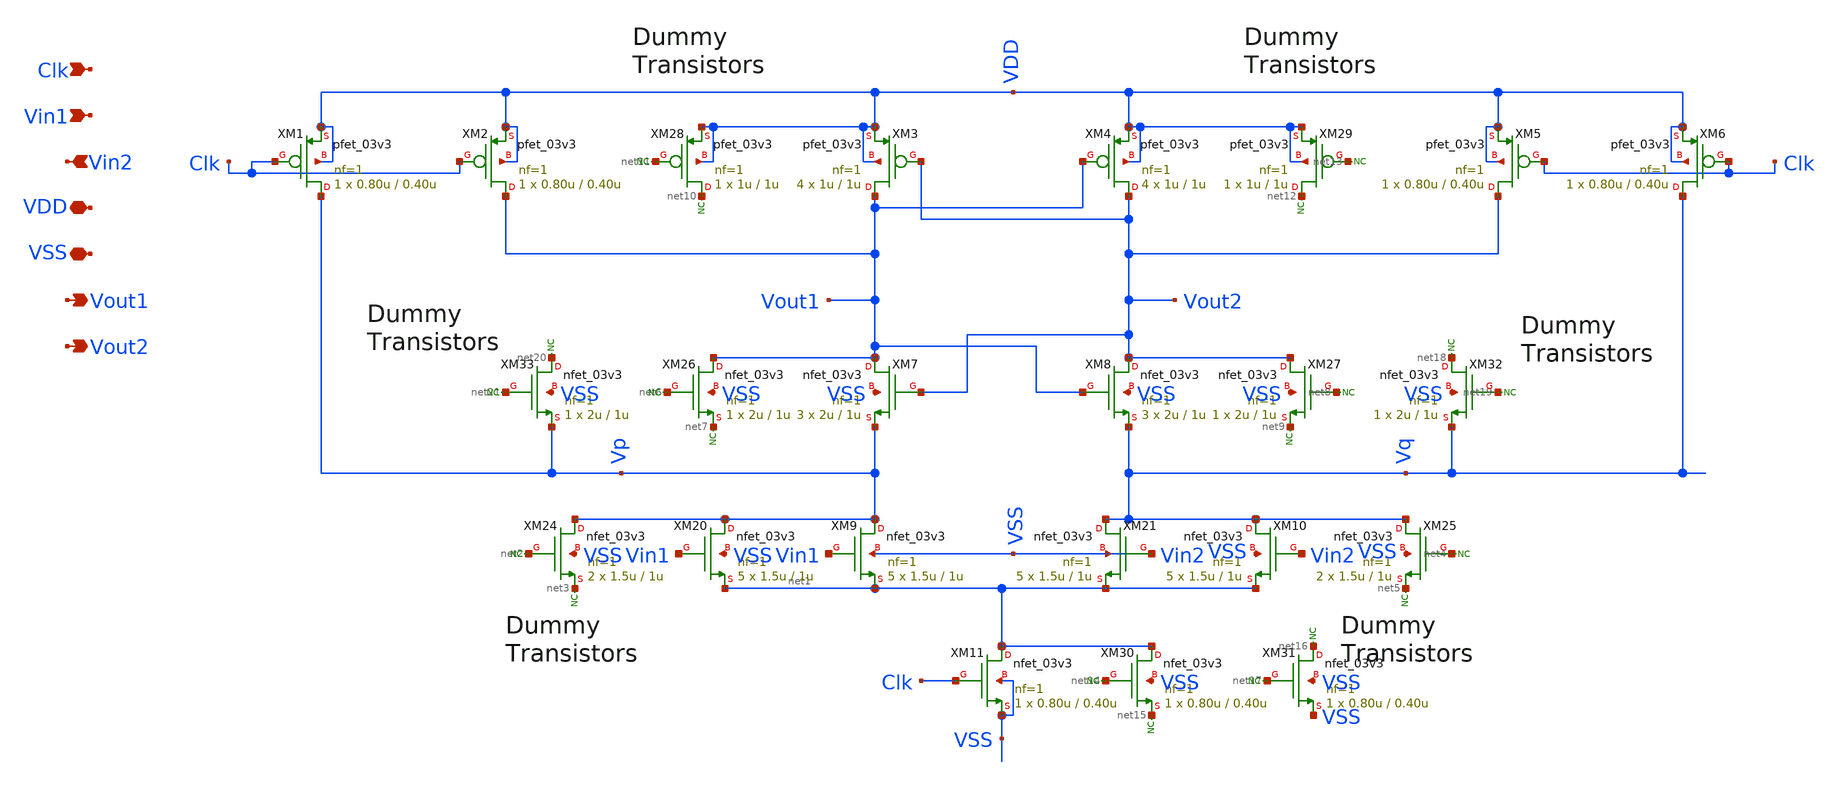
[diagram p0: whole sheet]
** sch_path: designs/FinalBlocksLayout/no_offsetLatch/no_offsetLatch.sch
**.subckt no_offsetLatch Clk Vin1 Vin2 VDD VSS Vout1 Vout2
*.ipin Clk
*.ipin Vin1
*.ipin Vin2
*.iopin VDD
*.iopin VSS
*.opin Vout1
*.opin Vout2
XM1 Vp Clk VDD VDD pfet_03v3 L=0.40u W=0.80u nf=1 ad='int((nf+1)/2) * W/nf * 0.18u' as='int((nf+2)/2) * W/nf * 0.18u'
+ pd='2*int((nf+1)/2) * (W/nf + 0.18u)' ps='2*int((nf+2)/2) * (W/nf + 0.18u)' nrd='0.18u / W' nrs='0.18u / W'
+ sa=0 sb=0 sd=0 m=1
XM2 Vout1 Clk VDD VDD pfet_03v3 L=0.40u W=0.80u nf=1 ad='int((nf+1)/2) * W/nf * 0.18u' as='int((nf+2)/2) * W/nf * 0.18u'
+ pd='2*int((nf+1)/2) * (W/nf + 0.18u)' ps='2*int((nf+2)/2) * (W/nf + 0.18u)' nrd='0.18u / W' nrs='0.18u / W'
+ sa=0 sb=0 sd=0 m=1
XM3 Vout1 Vout2 VDD VDD pfet_03v3 L=1u W=1u nf=1 ad='int((nf+1)/2) * W/nf * 0.18u' as='int((nf+2)/2) * W/nf * 0.18u'
+ pd='2*int((nf+1)/2) * (W/nf + 0.18u)' ps='2*int((nf+2)/2) * (W/nf + 0.18u)' nrd='0.18u / W' nrs='0.18u / W'
+ sa=0 sb=0 sd=0 m=4
XM4 Vout2 Vout1 VDD VDD pfet_03v3 L=1u W=1u nf=1 ad='int((nf+1)/2) * W/nf * 0.18u' as='int((nf+2)/2) * W/nf * 0.18u'
+ pd='2*int((nf+1)/2) * (W/nf + 0.18u)' ps='2*int((nf+2)/2) * (W/nf + 0.18u)' nrd='0.18u / W' nrs='0.18u / W'
+ sa=0 sb=0 sd=0 m=4
XM5 Vout2 Clk VDD VDD pfet_03v3 L=0.40u W=0.80u nf=1 ad='int((nf+1)/2) * W/nf * 0.18u' as='int((nf+2)/2) * W/nf * 0.18u'
+ pd='2*int((nf+1)/2) * (W/nf + 0.18u)' ps='2*int((nf+2)/2) * (W/nf + 0.18u)' nrd='0.18u / W' nrs='0.18u / W'
+ sa=0 sb=0 sd=0 m=1
XM6 Vq Clk VDD VDD pfet_03v3 L=0.40u W=0.80u nf=1 ad='int((nf+1)/2) * W/nf * 0.18u' as='int((nf+2)/2) * W/nf * 0.18u'
+ pd='2*int((nf+1)/2) * (W/nf + 0.18u)' ps='2*int((nf+2)/2) * (W/nf + 0.18u)' nrd='0.18u / W' nrs='0.18u / W'
+ sa=0 sb=0 sd=0 m=1
XM7 Vout1 Vout2 Vp VSS nfet_03v3 L=1u W=2u nf=1 ad='int((nf+1)/2) * W/nf * 0.18u' as='int((nf+2)/2) * W/nf * 0.18u'
+ pd='2*int((nf+1)/2) * (W/nf + 0.18u)' ps='2*int((nf+2)/2) * (W/nf + 0.18u)' nrd='0.18u / W' nrs='0.18u / W'
+ sa=0 sb=0 sd=0 m=3
XM8 Vout2 Vout1 Vq VSS nfet_03v3 L=1u W=2u nf=1 ad='int((nf+1)/2) * W/nf * 0.18u' as='int((nf+2)/2) * W/nf * 0.18u'
+ pd='2*int((nf+1)/2) * (W/nf + 0.18u)' ps='2*int((nf+2)/2) * (W/nf + 0.18u)' nrd='0.18u / W' nrs='0.18u / W'
+ sa=0 sb=0 sd=0 m=3
XM9 Vp Vin1 net1 VSS nfet_03v3 L=1u W=1.5u nf=1 ad='int((nf+1)/2) * W/nf * 0.18u' as='int((nf+2)/2) * W/nf * 0.18u'
+ pd='2*int((nf+1)/2) * (W/nf + 0.18u)' ps='2*int((nf+2)/2) * (W/nf + 0.18u)' nrd='0.18u / W' nrs='0.18u / W'
+ sa=0 sb=0 sd=0 m=5
XM10 Vq Vin2 net1 VSS nfet_03v3 L=1u W=1.5u nf=1 ad='int((nf+1)/2) * W/nf * 0.18u' as='int((nf+2)/2) * W/nf * 0.18u'
+ pd='2*int((nf+1)/2) * (W/nf + 0.18u)' ps='2*int((nf+2)/2) * (W/nf + 0.18u)' nrd='0.18u / W' nrs='0.18u / W'
+ sa=0 sb=0 sd=0 m=5
XM11 net1 Clk VSS VSS nfet_03v3 L=0.40u W=0.80u nf=1 ad='int((nf+1)/2) * W/nf * 0.18u' as='int((nf+2)/2) * W/nf * 0.18u'
+ pd='2*int((nf+1)/2) * (W/nf + 0.18u)' ps='2*int((nf+2)/2) * (W/nf + 0.18u)' nrd='0.18u / W' nrs='0.18u / W'
+ sa=0 sb=0 sd=0 m=1
XM20 Vp Vin1 net1 VSS nfet_03v3 L=1u W=1.5u nf=1 ad='int((nf+1)/2) * W/nf * 0.18u' as='int((nf+2)/2) * W/nf * 0.18u'
+ pd='2*int((nf+1)/2) * (W/nf + 0.18u)' ps='2*int((nf+2)/2) * (W/nf + 0.18u)' nrd='0.18u / W' nrs='0.18u / W'
+ sa=0 sb=0 sd=0 m=5
XM21 Vq Vin2 net1 VSS nfet_03v3 L=1u W=1.5u nf=1 ad='int((nf+1)/2) * W/nf * 0.18u' as='int((nf+2)/2) * W/nf * 0.18u'
+ pd='2*int((nf+1)/2) * (W/nf + 0.18u)' ps='2*int((nf+2)/2) * (W/nf + 0.18u)' nrd='0.18u / W' nrs='0.18u / W'
+ sa=0 sb=0 sd=0 m=5
XM24 Vp net2 net3 VSS nfet_03v3 L=1u W=1.5u nf=1 ad='int((nf+1)/2) * W/nf * 0.18u' as='int((nf+2)/2) * W/nf * 0.18u'
+ pd='2*int((nf+1)/2) * (W/nf + 0.18u)' ps='2*int((nf+2)/2) * (W/nf + 0.18u)' nrd='0.18u / W' nrs='0.18u / W'
+ sa=0 sb=0 sd=0 m=2
* noconn #net3
* noconn #net2
XM25 Vq net4 net5 VSS nfet_03v3 L=1u W=1.5u nf=1 ad='int((nf+1)/2) * W/nf * 0.18u' as='int((nf+2)/2) * W/nf * 0.18u'
+ pd='2*int((nf+1)/2) * (W/nf + 0.18u)' ps='2*int((nf+2)/2) * (W/nf + 0.18u)' nrd='0.18u / W' nrs='0.18u / W'
+ sa=0 sb=0 sd=0 m=2
* noconn #net5
* noconn #net4
XM26 Vout1 net6 net7 VSS nfet_03v3 L=1u W=2u nf=1 ad='int((nf+1)/2) * W/nf * 0.18u' as='int((nf+2)/2) * W/nf * 0.18u'
+ pd='2*int((nf+1)/2) * (W/nf + 0.18u)' ps='2*int((nf+2)/2) * (W/nf + 0.18u)' nrd='0.18u / W' nrs='0.18u / W'
+ sa=0 sb=0 sd=0 m=1
* noconn #net7
* noconn #net6
XM27 Vout2 net8 net9 VSS nfet_03v3 L=1u W=2u nf=1 ad='int((nf+1)/2) * W/nf * 0.18u' as='int((nf+2)/2) * W/nf * 0.18u'
+ pd='2*int((nf+1)/2) * (W/nf + 0.18u)' ps='2*int((nf+2)/2) * (W/nf + 0.18u)' nrd='0.18u / W' nrs='0.18u / W'
+ sa=0 sb=0 sd=0 m=1
* noconn #net9
* noconn #net8
* noconn #net10
* noconn #net11
* noconn #net12
* noconn #net13
XM30 net1 net14 net15 VSS nfet_03v3 L=0.40u W=0.80u nf=1 ad='int((nf+1)/2) * W/nf * 0.18u' as='int((nf+2)/2) * W/nf * 0.18u'
+ pd='2*int((nf+1)/2) * (W/nf + 0.18u)' ps='2*int((nf+2)/2) * (W/nf + 0.18u)' nrd='0.18u / W' nrs='0.18u / W'
+ sa=0 sb=0 sd=0 m=1
XM31 net16 net17 VSS VSS nfet_03v3 L=0.40u W=0.80u nf=1 ad='int((nf+1)/2) * W/nf * 0.18u' as='int((nf+2)/2) * W/nf * 0.18u'
+ pd='2*int((nf+1)/2) * (W/nf + 0.18u)' ps='2*int((nf+2)/2) * (W/nf + 0.18u)' nrd='0.18u / W' nrs='0.18u / W'
+ sa=0 sb=0 sd=0 m=1
* noconn #net15
* noconn #net16
* noconn #net17
* noconn #net14
XM32 net18 net19 Vq VSS nfet_03v3 L=1u W=2u nf=1 ad='int((nf+1)/2) * W/nf * 0.18u' as='int((nf+2)/2) * W/nf * 0.18u'
+ pd='2*int((nf+1)/2) * (W/nf + 0.18u)' ps='2*int((nf+2)/2) * (W/nf + 0.18u)' nrd='0.18u / W' nrs='0.18u / W'
+ sa=0 sb=0 sd=0 m=1
* noconn #net18
* noconn #net19
XM33 net20 net21 Vp VSS nfet_03v3 L=1u W=2u nf=1 ad='int((nf+1)/2) * W/nf * 0.18u' as='int((nf+2)/2) * W/nf * 0.18u'
+ pd='2*int((nf+1)/2) * (W/nf + 0.18u)' ps='2*int((nf+2)/2) * (W/nf + 0.18u)' nrd='0.18u / W' nrs='0.18u / W'
+ sa=0 sb=0 sd=0 m=1
* noconn #net20
* noconn #net21
XM28 net10 net11 VDD VDD pfet_03v3 L=1u W=1u nf=1 ad='int((nf+1)/2) * W/nf * 0.18u' as='int((nf+2)/2) * W/nf * 0.18u'
+ pd='2*int((nf+1)/2) * (W/nf + 0.18u)' ps='2*int((nf+2)/2) * (W/nf + 0.18u)' nrd='0.18u / W' nrs='0.18u / W'
+ sa=0 sb=0 sd=0 m=1
XM29 net12 net13 VDD VDD pfet_03v3 L=1u W=1u nf=1 ad='int((nf+1)/2) * W/nf * 0.18u' as='int((nf+2)/2) * W/nf * 0.18u'
+ pd='2*int((nf+1)/2) * (W/nf + 0.18u)' ps='2*int((nf+2)/2) * (W/nf + 0.18u)' nrd='0.18u / W' nrs='0.18u / W'
+ sa=0 sb=0 sd=0 m=1
**.ends
.end
